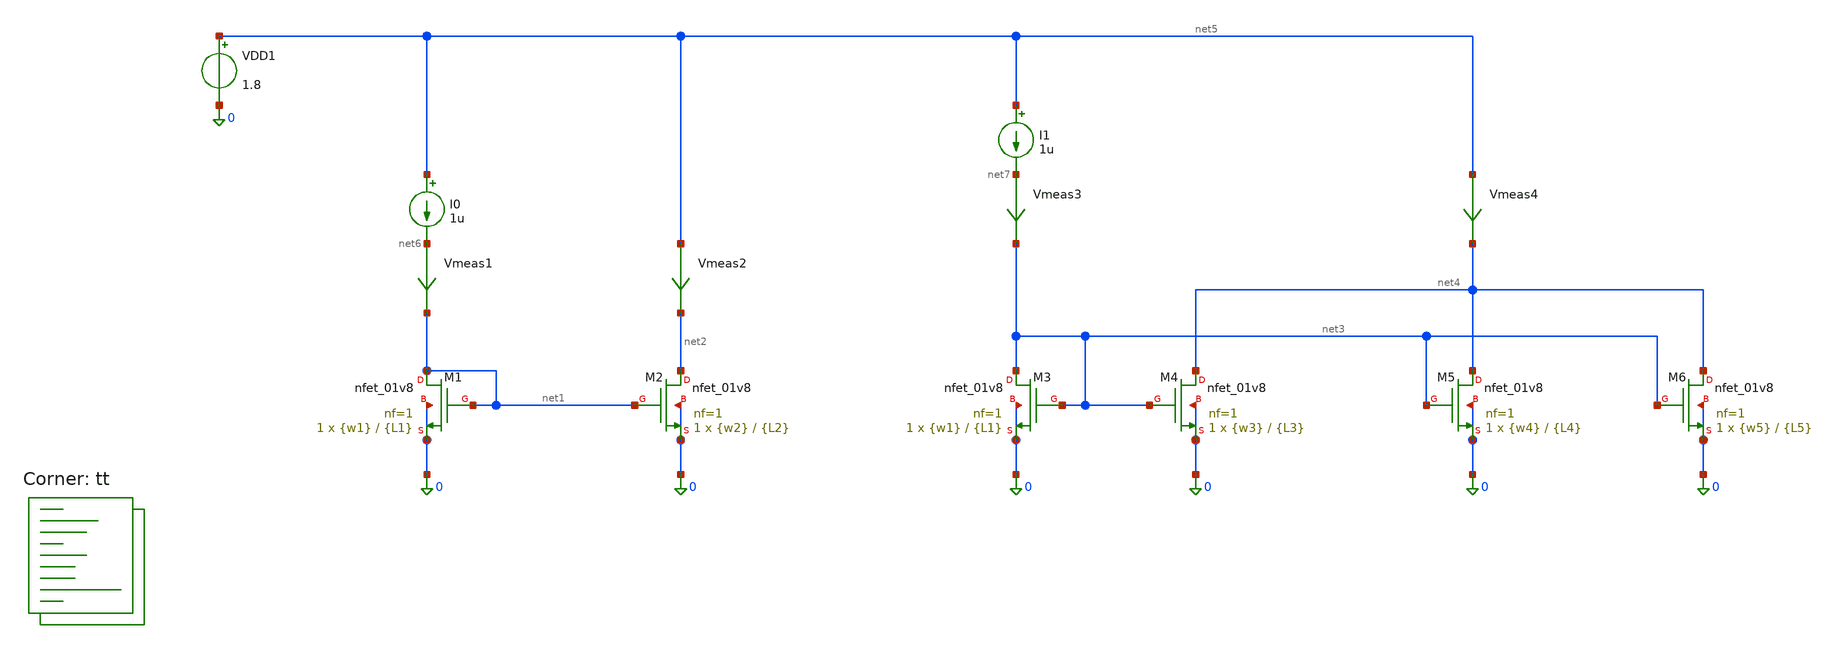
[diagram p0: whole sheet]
** sch_path: Training-3/conventional-cm.sch
**.subckt conventional-cm
XM1 net1 net1 0 0 sky130_fd_pr__nfet_01v8 L={L1} W={w1} nf=1 ad='int((nf+1)/2) * W/nf * 0.29' as='int((nf+2)/2) * W/nf * 0.29'
+ pd='2*int((nf+1)/2) * (W/nf + 0.29)' ps='2*int((nf+2)/2) * (W/nf + 0.29)' nrd='0.29 / W' nrs='0.29 / W'
+ sa=0 sb=0 sd=0 mult=1 m=1
XM2 net2 net1 0 0 sky130_fd_pr__nfet_01v8 L={L2} W={w2} nf=1 ad='int((nf+1)/2) * W/nf * 0.29' as='int((nf+2)/2) * W/nf * 0.29'
+ pd='2*int((nf+1)/2) * (W/nf + 0.29)' ps='2*int((nf+2)/2) * (W/nf + 0.29)' nrd='0.29 / W' nrs='0.29 / W'
+ sa=0 sb=0 sd=0 mult=1 m=1
XM3 net3 net3 0 0 sky130_fd_pr__nfet_01v8 L={L1} W={w1} nf=1 ad='int((nf+1)/2) * W/nf * 0.29' as='int((nf+2)/2) * W/nf * 0.29'
+ pd='2*int((nf+1)/2) * (W/nf + 0.29)' ps='2*int((nf+2)/2) * (W/nf + 0.29)' nrd='0.29 / W' nrs='0.29 / W'
+ sa=0 sb=0 sd=0 mult=1 m=1
XM4 net4 net3 0 0 sky130_fd_pr__nfet_01v8 L={L3} W={w3} nf=1 ad='int((nf+1)/2) * W/nf * 0.29' as='int((nf+2)/2) * W/nf * 0.29'
+ pd='2*int((nf+1)/2) * (W/nf + 0.29)' ps='2*int((nf+2)/2) * (W/nf + 0.29)' nrd='0.29 / W' nrs='0.29 / W'
+ sa=0 sb=0 sd=0 mult=1 m=1
XM5 net4 net3 0 0 sky130_fd_pr__nfet_01v8 L={L4} W={w4} nf=1 ad='int((nf+1)/2) * W/nf * 0.29' as='int((nf+2)/2) * W/nf * 0.29'
+ pd='2*int((nf+1)/2) * (W/nf + 0.29)' ps='2*int((nf+2)/2) * (W/nf + 0.29)' nrd='0.29 / W' nrs='0.29 / W'
+ sa=0 sb=0 sd=0 mult=1 m=1
XM6 net4 net3 0 0 sky130_fd_pr__nfet_01v8 L={L5} W={w5} nf=1 ad='int((nf+1)/2) * W/nf * 0.29' as='int((nf+2)/2) * W/nf * 0.29'
+ pd='2*int((nf+1)/2) * (W/nf + 0.29)' ps='2*int((nf+2)/2) * (W/nf + 0.29)' nrd='0.29 / W' nrs='0.29 / W'
+ sa=0 sb=0 sd=0 mult=1 m=1
Vmeas1 net6 net1 0
.save i(vmeas1)
Vmeas2 net5 net2 0
.save i(vmeas2)
Vmeas3 net7 net3 0
.save i(vmeas3)
Vmeas4 net5 net4 0
.save i(vmeas4)
VDD1 net5 0 1.8
I0 net5 net6 1u
I1 net5 net7 1u
**** begin user architecture code



.param L1 = 0.3
.param L2 = 0.3
.param L3 = 0.3
.param L4 = 0.3
.param L5 = 0.3

.param w1 = 3
.param w2 = 3
.param w3 = 3
.param w4 = 3
.param w5 = 3


.save
.control

*dc vdd1 0 1.8 0.01
*plot i(vmeas1) i(vmeas2) i(vmeas4)

tran 1n 100n
plot i(vmeas1) i(vmeas2) i(vmeas4)

op
let error1 = i(vmeas2)-i(vmeas1)
let error2 = i(vmeas4)-(i(vmeas1)*3)
print i(vmeas1) i(vmeas2) i(vmeas4)
print error1 error2

.endc




.lib $::SKYWATER_MODELS/sky130.lib.spice tt
**** end user architecture code
**.ends
.end
